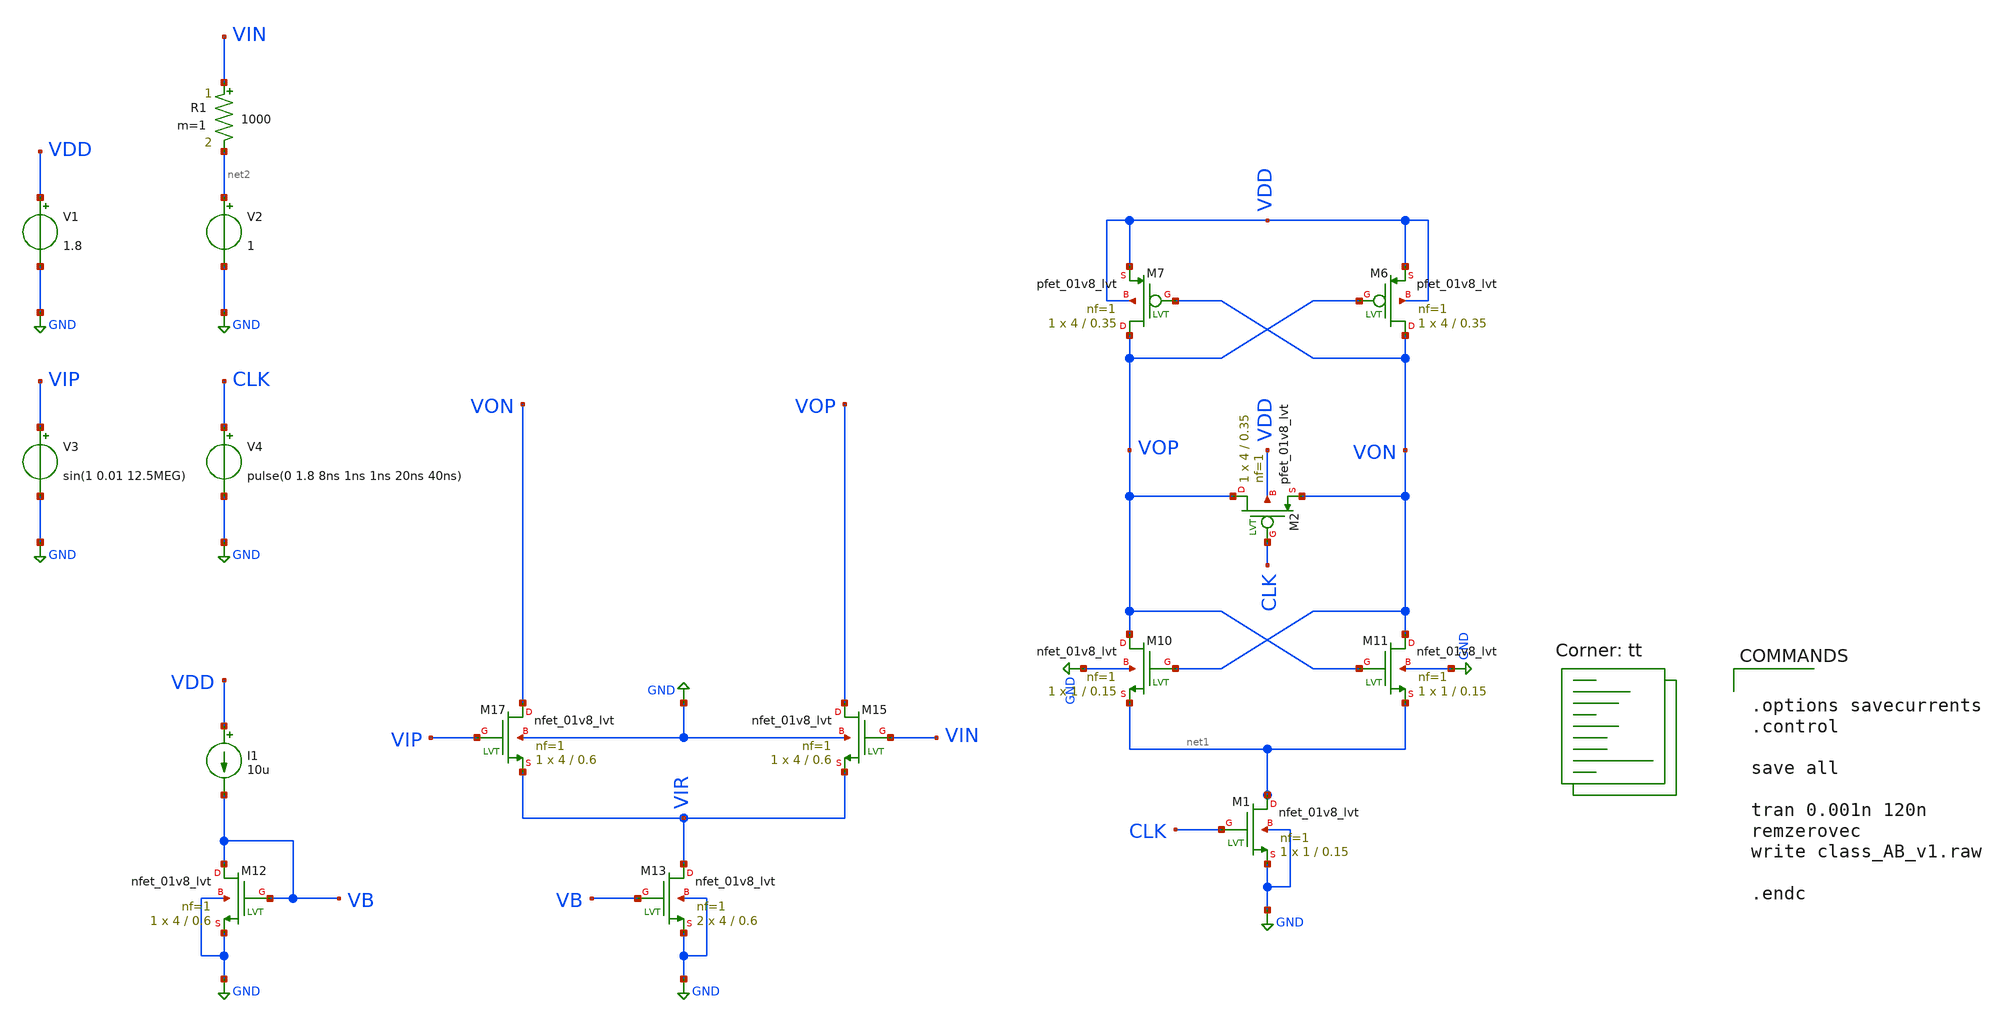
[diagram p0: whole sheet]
** sch_path: strongARM/class_AB_v1.sch
**.subckt class_AB_v1
XM17 VON VIP VIR GND sky130_fd_pr__nfet_01v8_lvt L=0.6 W=4 nf=1 ad='int((nf+1)/2) * W/nf * 0.29' as='int((nf+2)/2) * W/nf * 0.29'
+ pd='2*int((nf+1)/2) * (W/nf + 0.29)' ps='2*int((nf+2)/2) * (W/nf + 0.29)' nrd='0.29 / W' nrs='0.29 / W'
+ sa=0 sb=0 sd=0 mult=1 m=1
XM12 VB VB GND GND sky130_fd_pr__nfet_01v8_lvt L=0.6 W=4 nf=1 ad='int((nf+1)/2) * W/nf * 0.29' as='int((nf+2)/2) * W/nf * 0.29'
+ pd='2*int((nf+1)/2) * (W/nf + 0.29)' ps='2*int((nf+2)/2) * (W/nf + 0.29)' nrd='0.29 / W' nrs='0.29 / W'
+ sa=0 sb=0 sd=0 mult=1 m=1
I1 VDD VB 10u
XM15 VOP VIN VIR GND sky130_fd_pr__nfet_01v8_lvt L=0.6 W=4 nf=1 ad='int((nf+1)/2) * W/nf * 0.29' as='int((nf+2)/2) * W/nf * 0.29'
+ pd='2*int((nf+1)/2) * (W/nf + 0.29)' ps='2*int((nf+2)/2) * (W/nf + 0.29)' nrd='0.29 / W' nrs='0.29 / W'
+ sa=0 sb=0 sd=0 mult=1 m=1
XM13 VIR VB GND GND sky130_fd_pr__nfet_01v8_lvt L=0.6 W=4 nf=1 ad='int((nf+1)/2) * W/nf * 0.29' as='int((nf+2)/2) * W/nf * 0.29'
+ pd='2*int((nf+1)/2) * (W/nf + 0.29)' ps='2*int((nf+2)/2) * (W/nf + 0.29)' nrd='0.29 / W' nrs='0.29 / W'
+ sa=0 sb=0 sd=0 mult=2 m=2
XM6 VON VOP VDD VDD sky130_fd_pr__pfet_01v8_lvt L=0.35 W=4 nf=1 ad='int((nf+1)/2) * W/nf * 0.29' as='int((nf+2)/2) * W/nf * 0.29'
+ pd='2*int((nf+1)/2) * (W/nf + 0.29)' ps='2*int((nf+2)/2) * (W/nf + 0.29)' nrd='0.29 / W' nrs='0.29 / W'
+ sa=0 sb=0 sd=0 mult=1 m=1
XM7 VOP VON VDD VDD sky130_fd_pr__pfet_01v8_lvt L=0.35 W=4 nf=1 ad='int((nf+1)/2) * W/nf * 0.29' as='int((nf+2)/2) * W/nf * 0.29'
+ pd='2*int((nf+1)/2) * (W/nf + 0.29)' ps='2*int((nf+2)/2) * (W/nf + 0.29)' nrd='0.29 / W' nrs='0.29 / W'
+ sa=0 sb=0 sd=0 mult=1 m=1
XM10 VOP VON net1 GND sky130_fd_pr__nfet_01v8_lvt L=0.15 W=1 nf=1 ad='int((nf+1)/2) * W/nf * 0.29' as='int((nf+2)/2) * W/nf * 0.29'
+ pd='2*int((nf+1)/2) * (W/nf + 0.29)' ps='2*int((nf+2)/2) * (W/nf + 0.29)' nrd='0.29 / W' nrs='0.29 / W'
+ sa=0 sb=0 sd=0 mult=1 m=1
XM11 VON VOP net1 GND sky130_fd_pr__nfet_01v8_lvt L=0.15 W=1 nf=1 ad='int((nf+1)/2) * W/nf * 0.29' as='int((nf+2)/2) * W/nf * 0.29'
+ pd='2*int((nf+1)/2) * (W/nf + 0.29)' ps='2*int((nf+2)/2) * (W/nf + 0.29)' nrd='0.29 / W' nrs='0.29 / W'
+ sa=0 sb=0 sd=0 mult=1 m=1
XM1 net1 CLK GND GND sky130_fd_pr__nfet_01v8_lvt L=0.15 W=1 nf=1 ad='int((nf+1)/2) * W/nf * 0.29' as='int((nf+2)/2) * W/nf * 0.29'
+ pd='2*int((nf+1)/2) * (W/nf + 0.29)' ps='2*int((nf+2)/2) * (W/nf + 0.29)' nrd='0.29 / W' nrs='0.29 / W'
+ sa=0 sb=0 sd=0 mult=1 m=1
XM2 VOP CLK VON VDD sky130_fd_pr__pfet_01v8_lvt L=0.35 W=4 nf=1 ad='int((nf+1)/2) * W/nf * 0.29' as='int((nf+2)/2) * W/nf * 0.29'
+ pd='2*int((nf+1)/2) * (W/nf + 0.29)' ps='2*int((nf+2)/2) * (W/nf + 0.29)' nrd='0.29 / W' nrs='0.29 / W'
+ sa=0 sb=0 sd=0 mult=1 m=1
V1 VDD GND 1.8
V3 VIP GND sin(1 0.01 12.5MEG)
V2 net2 GND 1
V4 CLK GND pulse(0 1.8 8ns 1ns 1ns 20ns 40ns)
R1 VIN net2 1000 m=1
**** begin user architecture code
.lib $::SKYWATER_MODELS/sky130.lib.spice tt


.options savecurrents
.control

save all

tran 0.001n 120n
remzerovec
write class_AB_v1.raw

.endc


**** end user architecture code
**.ends
.GLOBAL GND
.end
